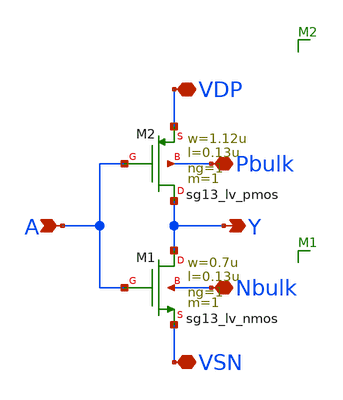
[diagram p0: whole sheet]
** sch_path: dependencies/CLK/CLK-main/schematic/xschem/ring_inv.sch
**.subckt ring_inv A Y Pbulk Nbulk VDP VSN
*.ipin A
*.opin Y
*.iopin Pbulk
*.iopin Nbulk
*.iopin VDP
*.iopin VSN
XM1 Y A VSN Nbulk sg13_lv_nmos w=0.7u l=0.13u ng=1 m=1 mm_ok=1
XM2 Y A VDP Pbulk sg13_lv_pmos w=1.12u l=0.13u ng=1 m=1 mm_ok=1
**.ends
.end
